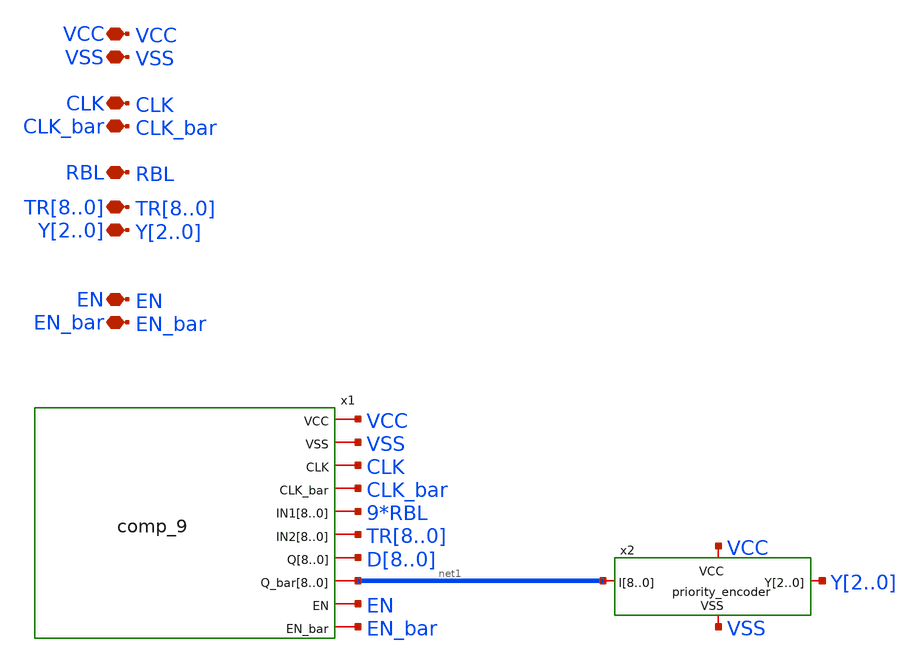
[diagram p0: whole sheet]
** sch_path: voltage_comp/MAC_decoder.sch
**.subckt MAC_decoder VSS VCC CLK CLK_bar EN EN_bar TR8,TR7,TR6,TR5,TR4,TR3,TR2,TR1,TR0 RBL Y2,Y1,Y0
*.iopin VSS
*.iopin VCC
*.iopin CLK
*.iopin CLK_bar
*.iopin EN
*.iopin EN_bar
*.iopin TR8,TR7,TR6,TR5,TR4,TR3,TR2,TR1,TR0
*.iopin RBL
*.iopin Y2,Y1,Y0
x1 VCC VSS CLK CLK_bar RBL RBL RBL RBL RBL RBL RBL RBL RBL TR8 TR7 TR6 TR5 TR4 TR3 TR2 TR1 TR0 D8 D7
+ D6 D5 D4 D3 D2 D1 D0 net1[8] net1[7] net1[6] net1[5] net1[4] net1[3] net1[2] net1[1] net1[0] EN EN_bar
+ comp_9
x2 VCC VSS net1[8] net1[7] net1[6] net1[5] net1[4] net1[3] net1[2] net1[1] net1[0] Y2 Y1 Y0
+ priority_encoder
**.ends
.end
